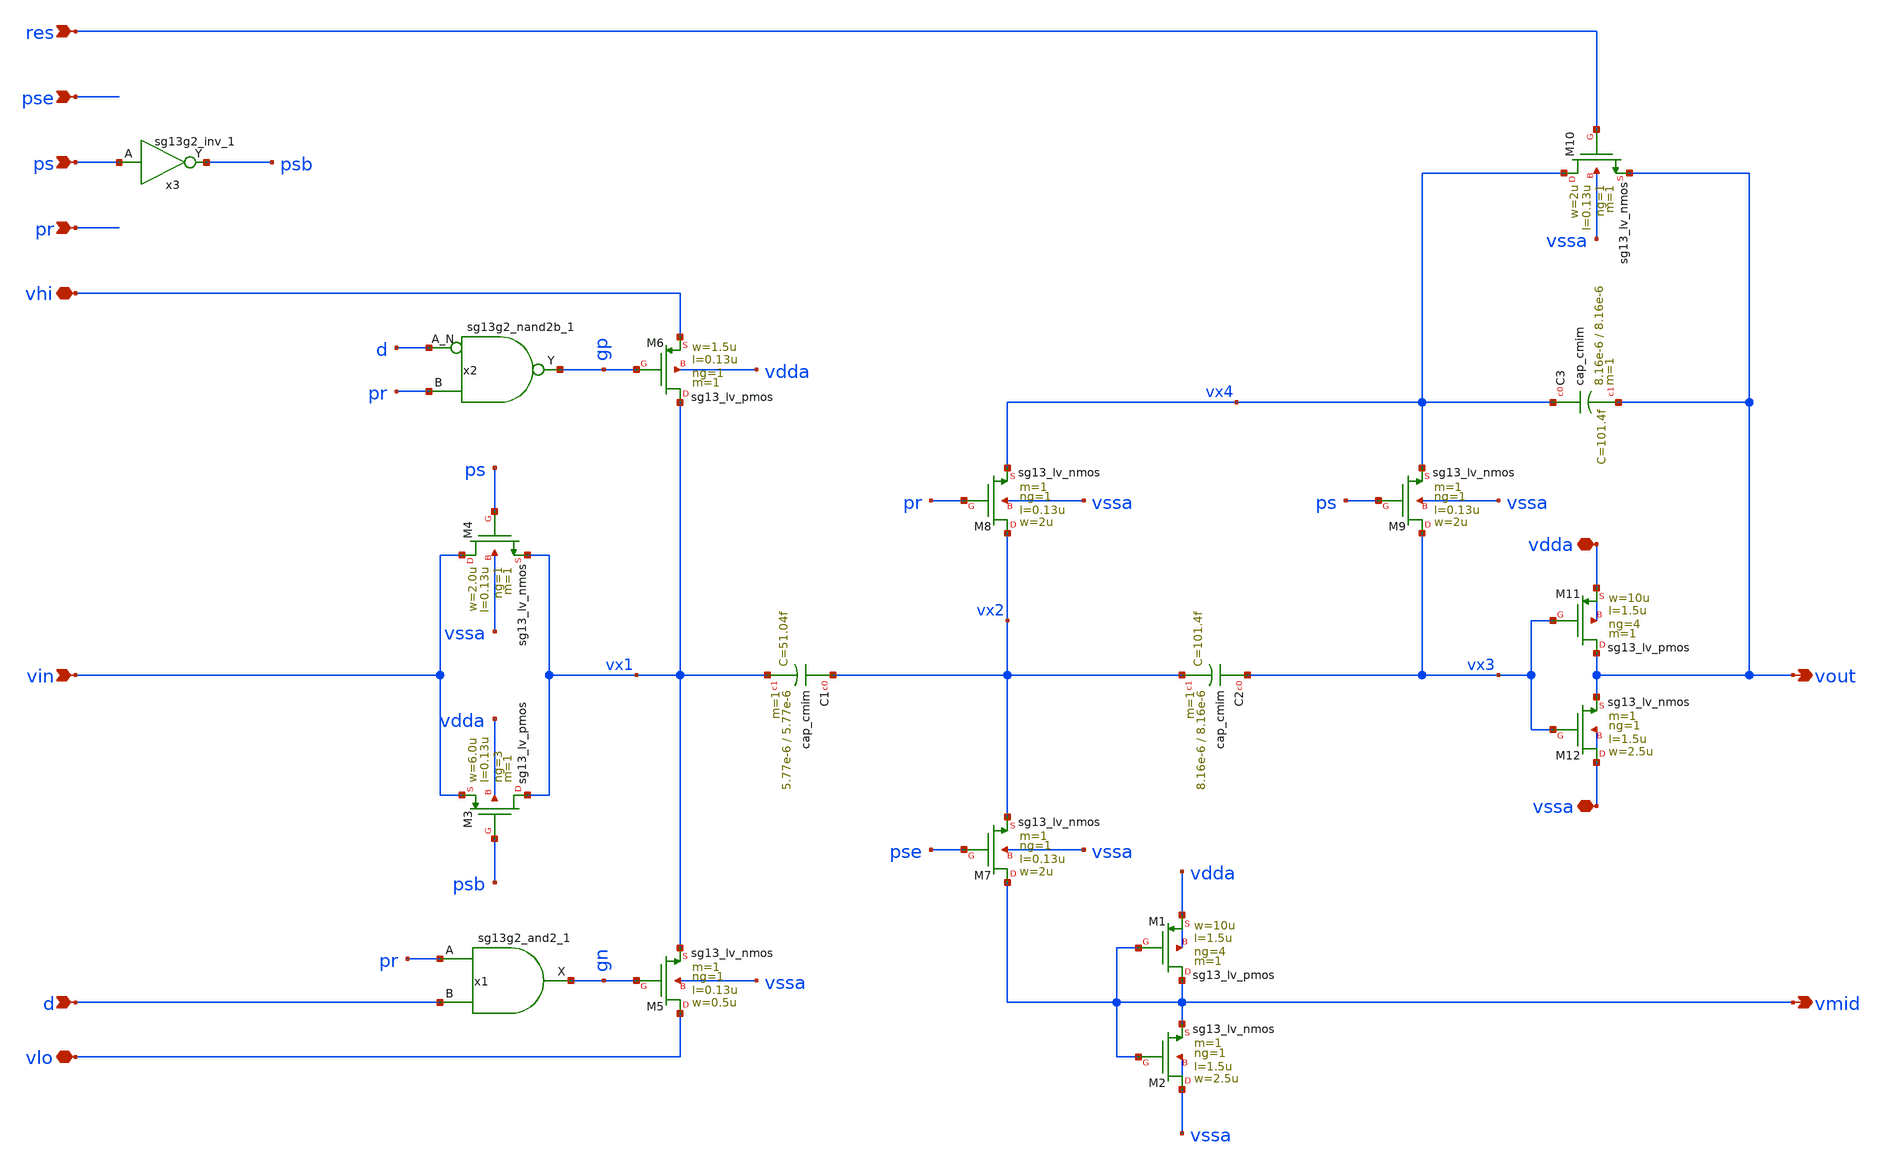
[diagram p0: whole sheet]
** sch_path: 5_Design/4_Layout/Team 6/xschem/stage_T6.sch
* IHP-GmbH/IHP-Open-PDK/ihp-sg13g2/libs.tech/xschem/sg13g2_stdcells/sg13g2_nand2b_1.sch:
* Copyright 2023 IHP PDK Authors
* Licensed under the Apache License, Version 2.0 (the "License");
**.subckt stage_T6 vhi pr vout d vin ps pse res vmid vlo vssa vdda
*.iopin vhi
*.ipin pr
*.opin vout
*.ipin d
*.ipin vin
*.ipin ps
*.ipin pse
*.ipin res
*.opin vmid
*.iopin vlo
*.iopin vssa
*.iopin vdda
x1 gn pr d VDD VSS sg13g2_and2_1
x2 gp d pr VDD VSS sg13g2_nand2b_1
XC1 vx2 vx1 cap_cmim w=5.77e-6 l=5.77e-6 m=1 mm_ok=1
XM3 vx1 psb vin vdda sg13_lv_pmos w=6.0u l=0.13u ng=3 m=1 mm_ok=1
XM4 vin ps vx1 vssa sg13_lv_nmos w=2.0u l=0.13u ng=1 m=1 mm_ok=1
XM5 vlo gn vx1 vssa sg13_lv_nmos w=0.5u l=0.13u ng=1 m=1 mm_ok=1
XM6 vx1 gp vhi vdda sg13_lv_pmos w=1.5u l=0.13u ng=1 m=1 mm_ok=1
XM7 vmid pse vx2 vssa sg13_lv_nmos w=2u l=0.13u ng=1 m=1 mm_ok=1
XM8 vx2 pr vx4 vssa sg13_lv_nmos w=2u l=0.13u ng=1 m=1 mm_ok=1
XC2 vx3 vx2 cap_cmim w=8.16e-6 l=8.16e-6 m=1 mm_ok=1
XM9 vx3 ps vx4 vssa sg13_lv_nmos w=2u l=0.13u ng=1 m=1 mm_ok=1
XC3 vx4 vout cap_cmim w=8.16e-6 l=8.16e-6 m=1 mm_ok=1
XM10 vx4 res vout vssa sg13_lv_nmos w=2u l=0.13u ng=1 m=1 mm_ok=1
XM11 vout vx3 vdda vdda sg13_lv_pmos w=10u l=1.5u ng=4 m=1 mm_ok=1
XM12 vssa vx3 vout vssa sg13_lv_nmos w=2.5u l=1.5u ng=1 m=1 mm_ok=1
XM1 vmid vmid vdda vdda sg13_lv_pmos w=10u l=1.5u ng=4 m=1 mm_ok=1
XM2 vssa vmid vmid vssa sg13_lv_nmos w=2.5u l=1.5u ng=1 m=1 mm_ok=1
x3 psb ps VDD VSS sg13g2_inv_1
**.ends

* expanding   symbol:  sg13g2_stdcells/sg13g2_and2_1.sym # of pins=3
** sym_path: sg13g2_stdcells/sg13g2_and2_1.sym
** sch_path: sg13g2_stdcells/sg13g2_and2_1.sch
.subckt sg13g2_and2_1 X A B VDD VSS
*.ipin A
*.ipin B
*.opin X
*.iopin VDD
*.iopin VSS
XM1 net1 A net2 VSS sg13_lv_nmos w=640.00n l=130.00n ng=1 m=1 mm_ok=1
XM2 net2 B VSS VSS sg13_lv_nmos w=640.00n l=130.00n ng=1 m=1 mm_ok=1
XM3 X net1 VSS VSS sg13_lv_nmos w=740.00n l=130.00n ng=1 m=1 mm_ok=1
XM4 net1 B VDD VDD sg13_lv_pmos w=840.00n l=130.00n ng=1 m=1 mm_ok=1
XM5 net1 A VDD VDD sg13_lv_pmos w=840.00n l=130.00n ng=1 m=1 mm_ok=1
XM6 X net1 VDD VDD sg13_lv_pmos w=1.12u l=130.00n ng=1 m=1 mm_ok=1
.ends


* expanding   symbol:  sg13g2_stdcells/sg13g2_nand2b_1.sym # of pins=3
** sym_path: sg13g2_stdcells/sg13g2_nand2b_1.sym
** sch_path: sg13g2_stdcells/sg13g2_nand2b_1.sch
.subckt sg13g2_nand2b_1 Y A_N B VDD VSS
*.opin Y
*.ipin B
*.ipin A_N
*.iopin VDD
*.iopin VSS
XM1 net1 A_N VSS VSS sg13_lv_nmos w=550.00n l=130.00n ng=1 m=1 mm_ok=1
XM2 Y net1 net2 VSS sg13_lv_nmos w=740.00n l=130.00n ng=1 m=1 mm_ok=1
XM3 net2 B VSS VSS sg13_lv_nmos w=740.00n l=130.00n ng=1 m=1 mm_ok=1
XM4 Y B VDD VDD sg13_lv_pmos w=1.12u l=130.00n ng=1 m=1 mm_ok=1
XM5 net1 A_N VDD VDD sg13_lv_pmos w=840.00n l=130.00n ng=1 m=1 mm_ok=1
XM6 Y net1 VDD VDD sg13_lv_pmos w=1.12u l=130.00n ng=1 m=1 mm_ok=1
.ends


* expanding   symbol:  sg13g2_stdcells/sg13g2_inv_1.sym # of pins=2
** sym_path: sg13g2_stdcells/sg13g2_inv_1.sym
** sch_path: sg13g2_stdcells/sg13g2_inv_1.sch
.subckt sg13g2_inv_1 Y A VDD VSS
*.opin Y
*.ipin A
*.iopin VDD
*.iopin VSS
XM1 Y A VSS VSS sg13_lv_nmos w=740.00n l=130.00n ng=1 m=1 mm_ok=1
XM2 Y A VDD VDD sg13_lv_pmos w=1.12u l=130.00n ng=1 m=1 mm_ok=1
.ends

.end
